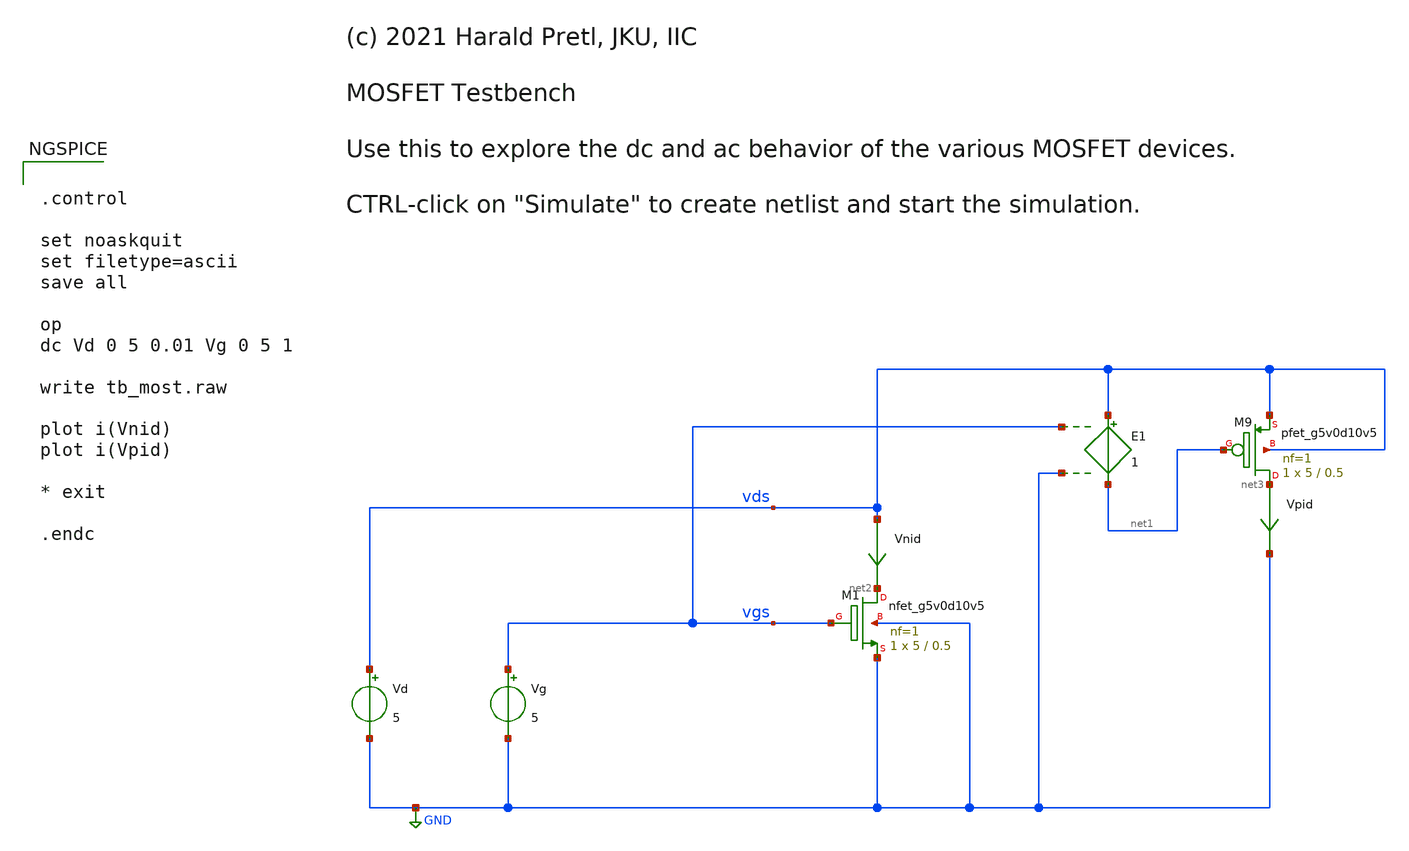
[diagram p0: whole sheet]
** sch_path: docs/examples/04a_analogue_circuit_layout_simulation/sky130nm/tb_most.sch
* (c) 2021 Harald Pretl, JKU, IIC
**.subckt tb_most
Vg vgs GND 5
Vd vds GND 5
XM1 net2 vgs GND GND sky130_fd_pr__nfet_g5v0d10v5 L=0.5 W=5 nf=1 ad='int((1 + 1)/2) * 5 / 1 * 0.29' as='int((1 + 2)/2) * 5 / 1 * 0.29'
+ pd='2*int((1 + 1)/2) * (5 / 1 + 0.29)' ps='2*int((1 + 2)/2) * (5 / 1 + 0.29)' nrd='0.29 / 5 ' nrs='0.29 / 5 '
+ sa=0 sb=0 sd=0 mult=1 m=1
XM9 net3 net1 vds vds sky130_fd_pr__pfet_g5v0d10v5 L=0.5 W=5 nf=1 ad='int((1 + 1)/2) * 5 / 1 * 0.29'
+ as='int((1 + 2)/2) * 5 / 1 * 0.29' pd='2*int((1 + 1)/2) * (5 / 1 + 0.29)' ps='2*int((1 + 2)/2) * (5 / 1 + 0.29)'
+ nrd='0.29 / 5 ' nrs='0.29 / 5 ' sa=0 sb=0 sd=0 mult=1 m=1
E1 vds net1 vgs GND 1
Vpid net3 GND 0
.save i(vpid)
Vnid vds net2 0
.save i(vnid)
**** begin user architecture code
 ** manual skywater pdks install (with patches applied)
* .lib $::SKYWATER_MODELS/models/sky130.lib.spice tt

** opencircuitdesign pdks install
.lib $::SKYWATER_MODELS/sky130.lib.spice.tt.red tt

.param mc_mm_switch=0
.param mc_pr_switch=0



.control

set noaskquit
set filetype=ascii
save all

op
dc Vd 0 5 0.01 Vg 0 5 1

write tb_most.raw

plot i(Vnid)
plot i(Vpid)

* exit

.endc


**** end user architecture code
**.ends
.GLOBAL GND
.end
